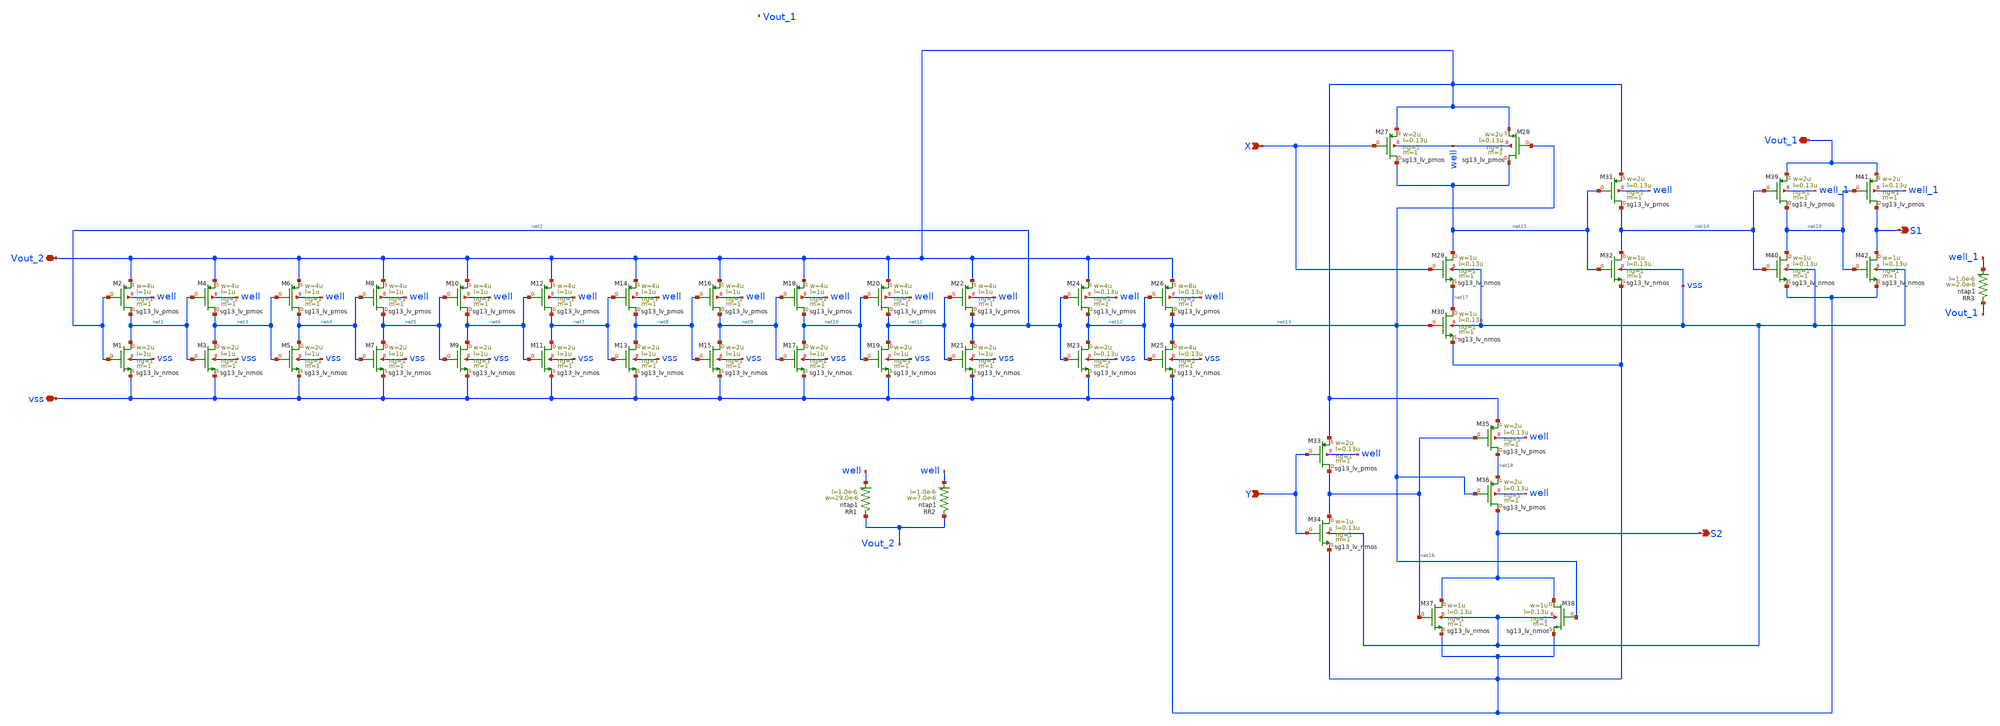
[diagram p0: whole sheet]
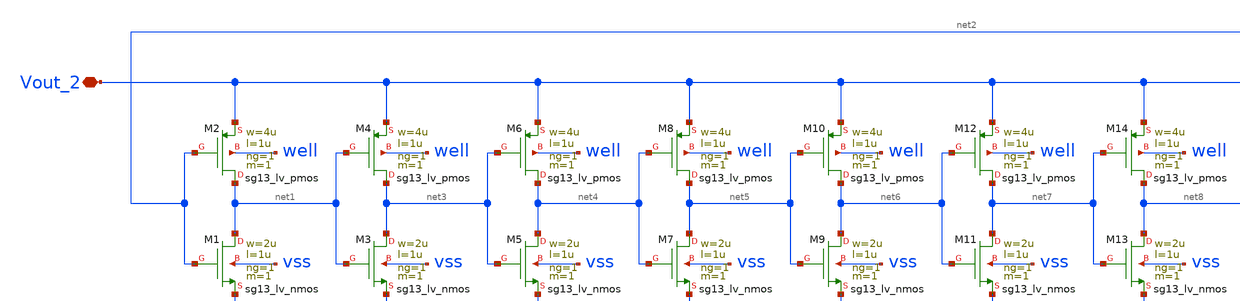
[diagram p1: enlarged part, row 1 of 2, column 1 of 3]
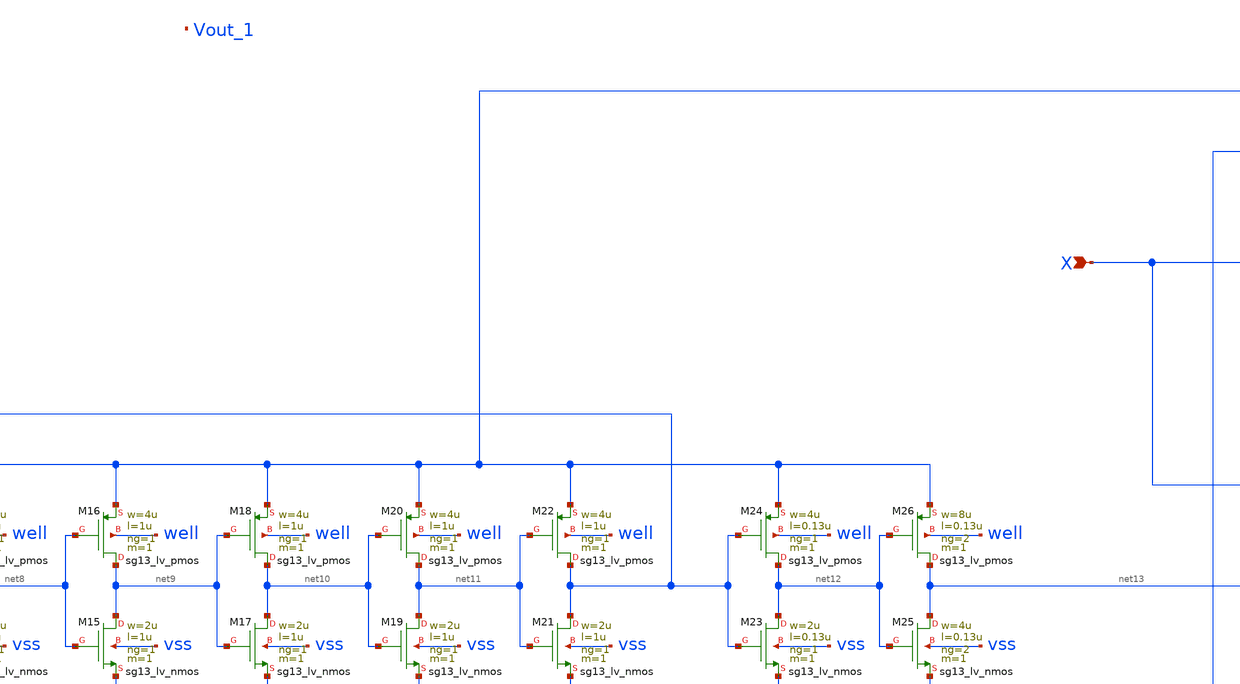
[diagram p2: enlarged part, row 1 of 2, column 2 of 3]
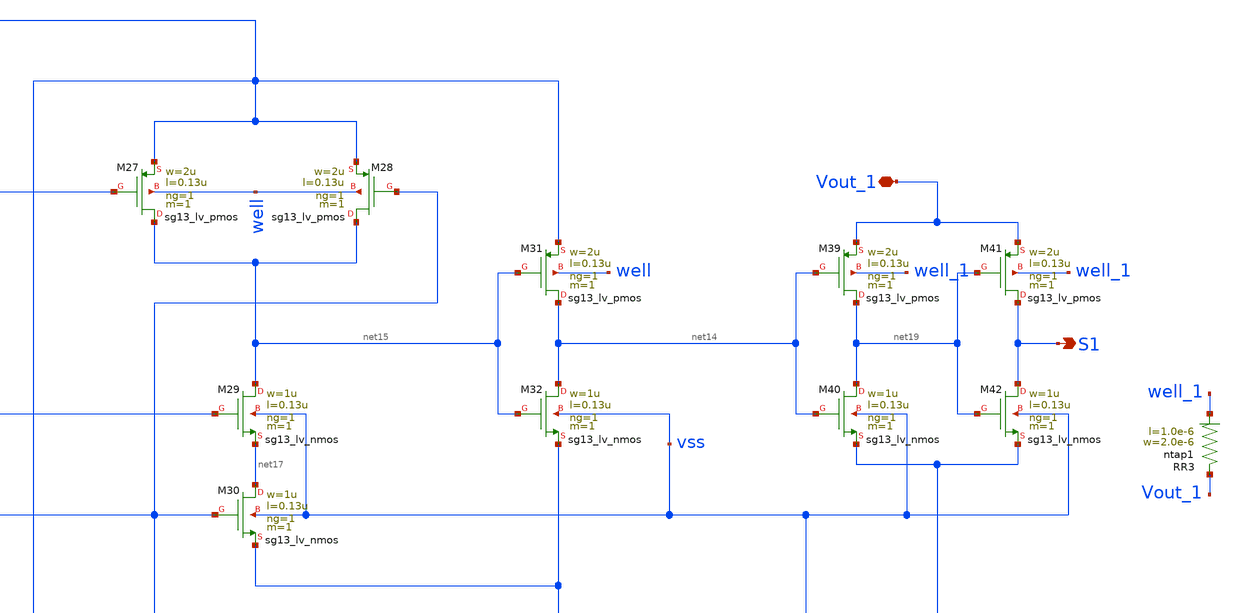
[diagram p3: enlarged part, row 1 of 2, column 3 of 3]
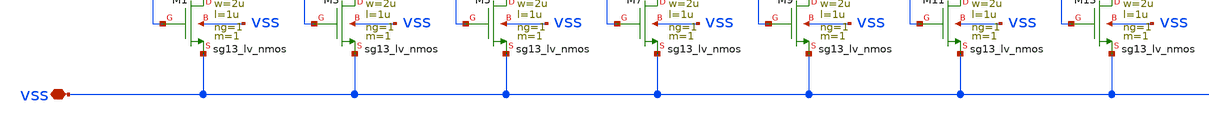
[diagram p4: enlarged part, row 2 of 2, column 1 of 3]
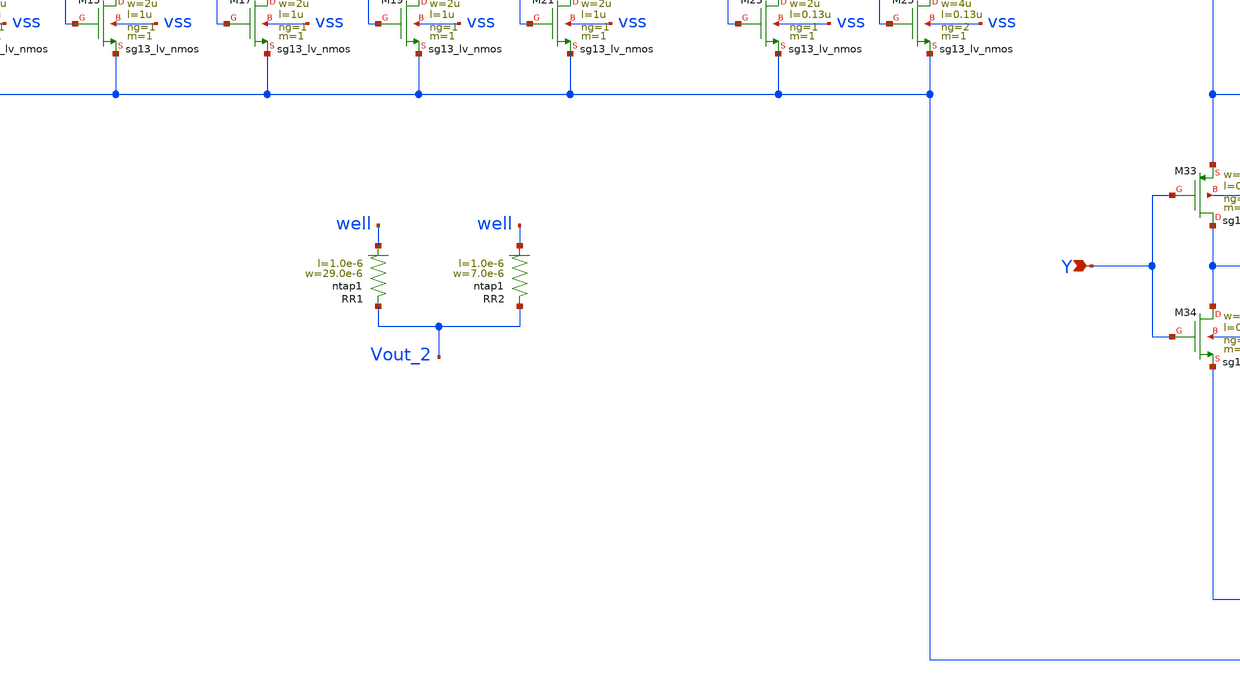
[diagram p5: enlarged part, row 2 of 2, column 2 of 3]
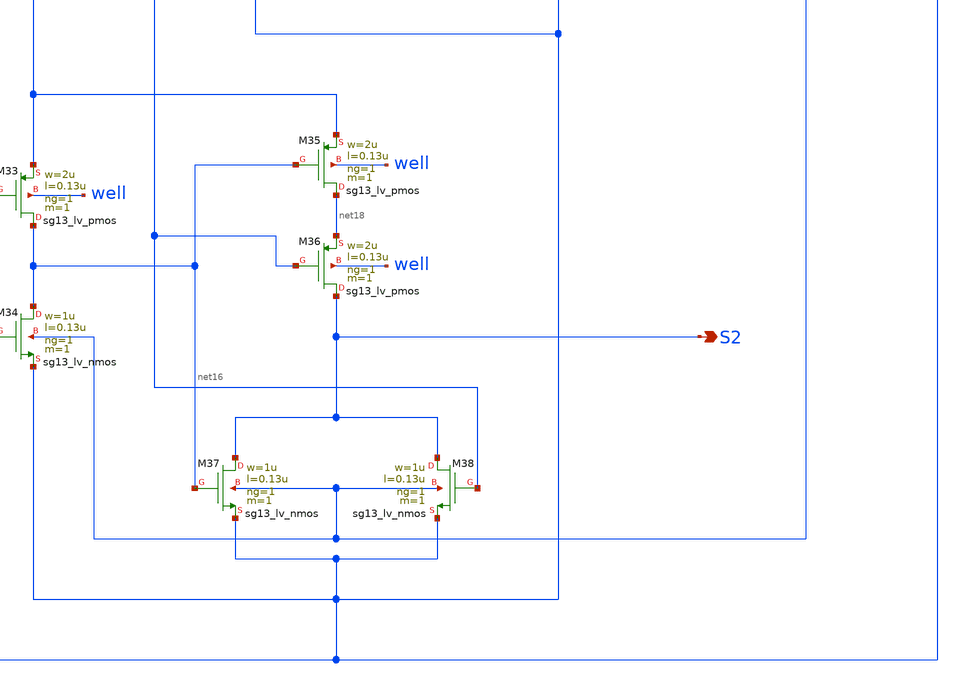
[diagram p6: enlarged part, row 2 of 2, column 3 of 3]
** sch_path: Layouts/Dig_control/dig_control_block2.sch
**.subckt dig_control_block2 Vout_2 vss X Y S2 S1 Vout_1
*.iopin Vout_2
*.iopin vss
*.ipin X
*.ipin Y
*.opin S2
*.opin S1
*.iopin Vout_1
XM1 net1 net2 vss vss sg13_lv_nmos w=2u l=1u ng=1 m=1 mm_ok=1
XM2 net1 net2 Vout_2 well sg13_lv_pmos w=4u l=1u ng=1 m=1 mm_ok=1
XM3 net3 net1 vss vss sg13_lv_nmos w=2u l=1u ng=1 m=1 mm_ok=1
XM4 net3 net1 Vout_2 well sg13_lv_pmos w=4u l=1u ng=1 m=1 mm_ok=1
XM5 net4 net3 vss vss sg13_lv_nmos w=2u l=1u ng=1 m=1 mm_ok=1
XM6 net4 net3 Vout_2 well sg13_lv_pmos w=4u l=1u ng=1 m=1 mm_ok=1
XM7 net5 net4 vss vss sg13_lv_nmos w=2u l=1u ng=1 m=1 mm_ok=1
XM8 net5 net4 Vout_2 well sg13_lv_pmos w=4u l=1u ng=1 m=1 mm_ok=1
XM9 net6 net5 vss vss sg13_lv_nmos w=2u l=1u ng=1 m=1 mm_ok=1
XM10 net6 net5 Vout_2 well sg13_lv_pmos w=4u l=1u ng=1 m=1 mm_ok=1
XM11 net7 net6 vss vss sg13_lv_nmos w=2u l=1u ng=1 m=1 mm_ok=1
XM12 net7 net6 Vout_2 well sg13_lv_pmos w=4u l=1u ng=1 m=1 mm_ok=1
XM13 net8 net7 vss vss sg13_lv_nmos w=2u l=1u ng=1 m=1 mm_ok=1
XM14 net8 net7 Vout_2 well sg13_lv_pmos w=4u l=1u ng=1 m=1 mm_ok=1
XM15 net9 net8 vss vss sg13_lv_nmos w=2u l=1u ng=1 m=1 mm_ok=1
XM16 net9 net8 Vout_2 well sg13_lv_pmos w=4u l=1u ng=1 m=1 mm_ok=1
XM17 net10 net9 vss vss sg13_lv_nmos w=2u l=1u ng=1 m=1 mm_ok=1
XM18 net10 net9 Vout_2 well sg13_lv_pmos w=4u l=1u ng=1 m=1 mm_ok=1
XM19 net11 net10 vss vss sg13_lv_nmos w=2u l=1u ng=1 m=1 mm_ok=1
XM20 net11 net10 Vout_2 well sg13_lv_pmos w=4u l=1u ng=1 m=1 mm_ok=1
XM21 net2 net11 vss vss sg13_lv_nmos w=2u l=1u ng=1 m=1 mm_ok=1
XM22 net2 net11 Vout_2 well sg13_lv_pmos w=4u l=1u ng=1 m=1 mm_ok=1
XM23 net12 net2 vss vss sg13_lv_nmos w=2u l=0.13u ng=1 m=1 mm_ok=1
XM24 net12 net2 Vout_2 well sg13_lv_pmos w=4u l=0.13u ng=1 m=1 mm_ok=1
XM26 net13 net12 Vout_2 well sg13_lv_pmos w=8u l=0.13u ng=2 m=1 mm_ok=1
XM25 net13 net12 vss vss sg13_lv_nmos w=4u l=0.13u ng=2 m=1 mm_ok=1
XR1 Vout_2 well ntap1 R=11.01 w=29.0e-6 l=1.0e-6
XM27 net15 X Vout_2 well sg13_lv_pmos w=2u l=0.13u ng=1 m=1 mm_ok=1
XM28 net15 net13 Vout_2 well sg13_lv_pmos w=2u l=0.13u ng=1 m=1 mm_ok=1
XM29 net15 X net17 vss sg13_lv_nmos w=1u l=0.13u ng=1 m=1 mm_ok=1
XM30 net17 net13 vss vss sg13_lv_nmos w=1u l=0.13u ng=1 m=1 mm_ok=1
XM31 net14 net15 Vout_2 well sg13_lv_pmos w=2u l=0.13u ng=1 m=1 mm_ok=1
XM32 net14 net15 vss vss sg13_lv_nmos w=1u l=0.13u ng=1 m=1 mm_ok=1
XM33 net16 Y Vout_2 well sg13_lv_pmos w=2u l=0.13u ng=1 m=1 mm_ok=1
XM34 net16 Y vss vss sg13_lv_nmos w=1u l=0.13u ng=1 m=1 mm_ok=1
XM35 net18 net16 Vout_2 well sg13_lv_pmos w=2u l=0.13u ng=1 m=1 mm_ok=1
XM36 S2 net13 net18 well sg13_lv_pmos w=2u l=0.13u ng=1 m=1 mm_ok=1
XM37 S2 net16 vss vss sg13_lv_nmos w=1u l=0.13u ng=1 m=1 mm_ok=1
XM38 S2 net13 vss vss sg13_lv_nmos w=1u l=0.13u ng=1 m=1 mm_ok=1
XR2 Vout_2 well ntap1 R=42.61 w=7.0e-6 l=1.0e-6
XM39 net19 net14 Vout_1 well_1 sg13_lv_pmos w=2u l=0.13u ng=1 m=1 mm_ok=1
XM40 net19 net14 vss vss sg13_lv_nmos w=1u l=0.13u ng=1 m=1 mm_ok=1
XM41 S1 net19 Vout_1 well_1 sg13_lv_pmos w=2u l=0.13u ng=1 m=1 mm_ok=1
XM42 S1 net19 vss vss sg13_lv_nmos w=1u l=0.13u ng=1 m=1 mm_ok=1
XR3 Vout_1 well_1 ntap1 R=122.5 w=2.0e-6 l=1.0e-6
**.ends
.end
